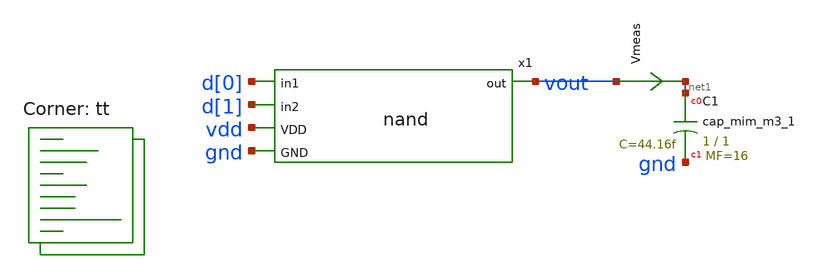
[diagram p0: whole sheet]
** sch_path: xschem/nand-tb.sch
**.subckt nand-tb
XC1 net1 gnd sky130_fd_pr__cap_mim_m3_1 W=1 L=1 MF=16 m=16
Vmeas vout net1 0
.save i(vmeas)
x1 d[0] d[1] vout vdd gnd nand
**** begin user architecture code
.lib $::SKYWATER_MODELS/sky130.lib.spice tt



  .option wnflag=1
  .option safecurrents
  ********************Static Voltage Sources***************************
  Vddh vdd gnd dc 1.8

  ********************Dynamic Voltage Sources***************************
  *******Calculation**********
  .param base_f=100e3 base_t={1/base_f} base_th={base_t/2} base_d={base_th}
  .param d2_th ={base_th} d2_t={2*d2_th}
  .param d1_th ={4*d2_th} d1_t={d0_th}
  .param d0_th ={4*d1_th} d0_t={4*d0_th}

  .param d20_d ={0} d21_d={1*d2_th} d22_d={2*d2_th} d23_d={3*d2_th}
  .param d10_d ={0} d11_d={1*d1_th} d12_d={2*d1_th} d13_d={3*d1_th}
  .param d00_d ={0} d01_d={1*d0_th} d02_d={2*d0_th} d03_d={3*d0_th}
  *******Signals**********
  .param vhi=1.8
  Vd00 d[0] gnd pulse(0 {vhi} {0} 1p 1p {10u} {20u})
  Vd01 d[1] gnd pulse(0 {vhi} {0} 1p 1p {20u} {40u})
  ********************Simulation Commands*****************************
  .control
     reset
     save all
     tran 1n 50u
     write nand-tb.raw
     set appendwrite
*    quit 0
  .endc



**** end user architecture code
**.ends

* expanding   symbol:  nand.sym # of pins=5
** sym_path: xschem/nand.sym
** sch_path: xschem/nand.sch
.subckt nand in1 in2 out VDD GND
*.ipin in2
*.opin out
*.ipin VDD
*.ipin GND
*.ipin in1
.param wp=0.63 wn=0.42 l=0.15
XM1 out in1 VDD VDD sky130_fd_pr__pfet_01v8 L=l W=wp nf=1 ad='int((nf+1)/2) * W/nf * 0.29' as='int((nf+2)/2) * W/nf * 0.29'
+ pd='2*int((nf+1)/2) * (W/nf + 0.29)' ps='2*int((nf+2)/2) * (W/nf + 0.29)' nrd='0.29 / W' nrs='0.29 / W'
+ sa=0 sb=0 sd=0 mult=1 m=1
XM2 out in2 VDD VDD sky130_fd_pr__pfet_01v8 L=l W=wp nf=1 ad='int((nf+1)/2) * W/nf * 0.29' as='int((nf+2)/2) * W/nf * 0.29'
+ pd='2*int((nf+1)/2) * (W/nf + 0.29)' ps='2*int((nf+2)/2) * (W/nf + 0.29)' nrd='0.29 / W' nrs='0.29 / W'
+ sa=0 sb=0 sd=0 mult=1 m=1
XM3 out in2 net1 GND sky130_fd_pr__nfet_01v8 L=l W=wn nf=1 ad='int((nf+1)/2) * W/nf * 0.29' as='int((nf+2)/2) * W/nf * 0.29'
+ pd='2*int((nf+1)/2) * (W/nf + 0.29)' ps='2*int((nf+2)/2) * (W/nf + 0.29)' nrd='0.29 / W' nrs='0.29 / W'
+ sa=0 sb=0 sd=0 mult=1 m=1
XM4 net1 in1 GND GND sky130_fd_pr__nfet_01v8 L=l W=wn nf=1 ad='int((nf+1)/2) * W/nf * 0.29' as='int((nf+2)/2) * W/nf * 0.29'
+ pd='2*int((nf+1)/2) * (W/nf + 0.29)' ps='2*int((nf+2)/2) * (W/nf + 0.29)' nrd='0.29 / W' nrs='0.29 / W'
+ sa=0 sb=0 sd=0 mult=1 m=1
.ends

.end
